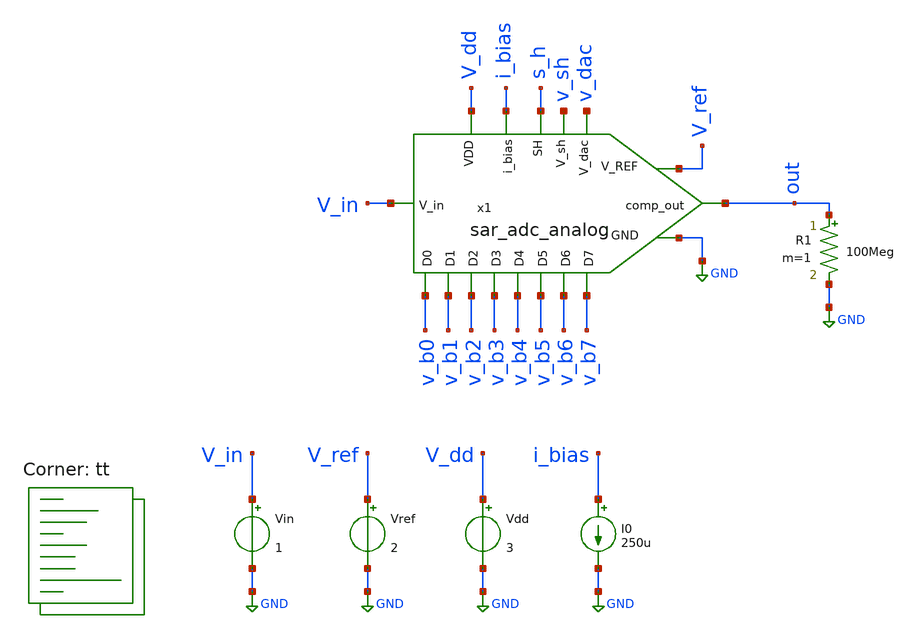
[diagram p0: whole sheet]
** sch_path: xschem/tb_sar_adc_analog.sch
**.subckt tb_sar_adc_analog
Vin V_in GND 1
x1 s_h V_in out i_bias v_b0 V_dd v_b1 v_b2 v_b3 GND v_b4 V_ref v_b5 v_b6 v_b7 v_sh v_dac
+ sar_adc_analog
Vref V_ref GND 2
R1 out GND 100Meg m=1
Vdd V_dd GND 3
I0 i_bias GND 250u
**** begin user architecture code
.lib $::SKYWATER_MODELS/sky130.lib.spice tt


.include "stimuli_tb_sar_adc_analog.cir"
.param v_hi = 1.8

.control

let index = 0


repeat 1
save all
tran 10p 172n
write tb_sar_adc_analog.raw
reset
end

.endc


**** end user architecture code
**.ends
.GLOBAL GND
.end
